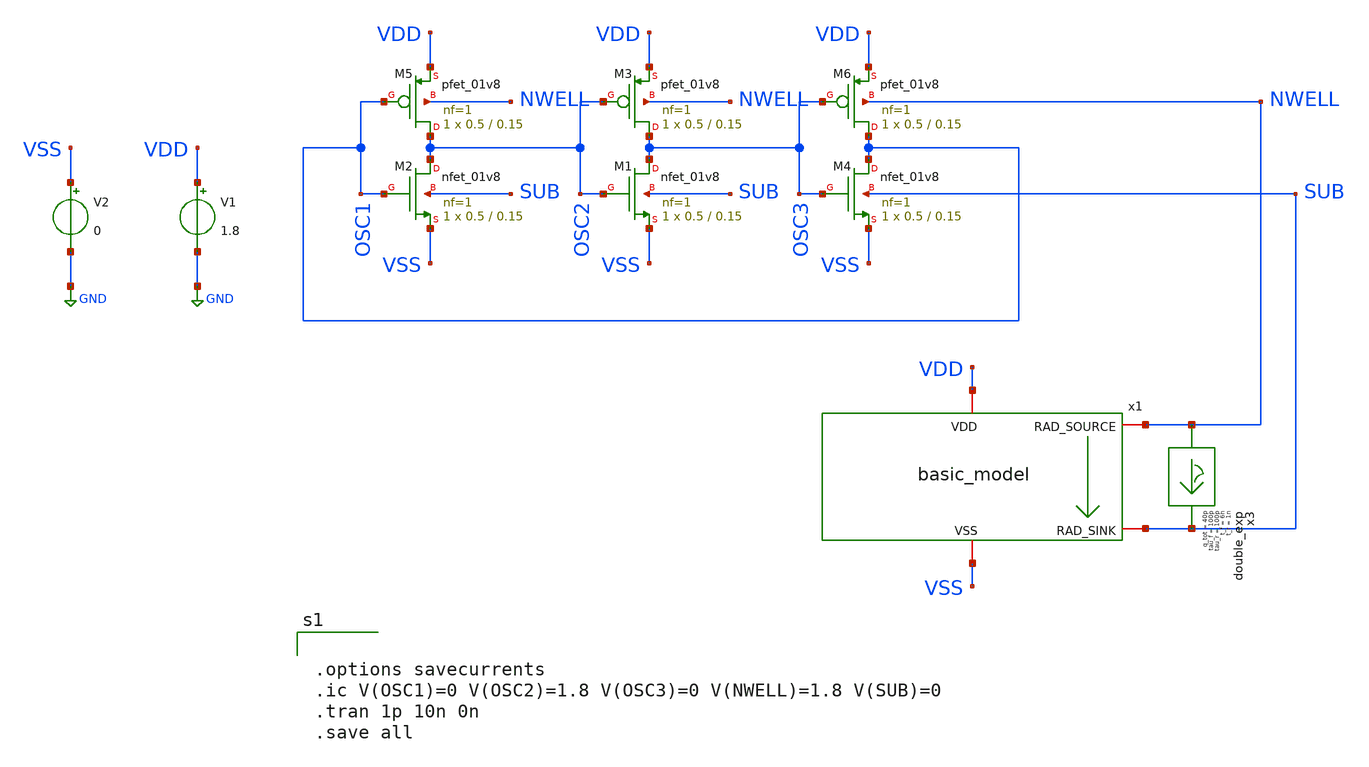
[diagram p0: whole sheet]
** sch_path: untitled-5.sch
**.subckt untitled-5
XM2 OSC2 OSC1 VSS SUB sky130_fd_pr__nfet_01v8 L=0.15 W=0.5 nf=1 ad='int((nf+1)/2) * W/nf * 0.29' as='int((nf+2)/2) * W/nf * 0.29'
+ pd='2*int((nf+1)/2) * (W/nf + 0.29)' ps='2*int((nf+2)/2) * (W/nf + 0.29)' nrd='0.29 / W' nrs='0.29 / W'
+ sa=0 sb=0 sd=0 mult=1 m=1
XM5 OSC2 OSC1 VDD NWELL sky130_fd_pr__pfet_01v8 L=0.15 W=0.5 nf=1 ad='int((nf+1)/2) * W/nf * 0.29' as='int((nf+2)/2) * W/nf * 0.29'
+ pd='2*int((nf+1)/2) * (W/nf + 0.29)' ps='2*int((nf+2)/2) * (W/nf + 0.29)' nrd='0.29 / W' nrs='0.29 / W'
+ sa=0 sb=0 sd=0 mult=1 m=1
XM1 OSC3 OSC2 VSS SUB sky130_fd_pr__nfet_01v8 L=0.15 W=0.5 nf=1 ad='int((nf+1)/2) * W/nf * 0.29' as='int((nf+2)/2) * W/nf * 0.29'
+ pd='2*int((nf+1)/2) * (W/nf + 0.29)' ps='2*int((nf+2)/2) * (W/nf + 0.29)' nrd='0.29 / W' nrs='0.29 / W'
+ sa=0 sb=0 sd=0 mult=1 m=1
XM3 OSC3 OSC2 VDD NWELL sky130_fd_pr__pfet_01v8 L=0.15 W=0.5 nf=1 ad='int((nf+1)/2) * W/nf * 0.29' as='int((nf+2)/2) * W/nf * 0.29'
+ pd='2*int((nf+1)/2) * (W/nf + 0.29)' ps='2*int((nf+2)/2) * (W/nf + 0.29)' nrd='0.29 / W' nrs='0.29 / W'
+ sa=0 sb=0 sd=0 mult=1 m=1
XM4 OSC1 OSC3 VSS SUB sky130_fd_pr__nfet_01v8 L=0.15 W=0.5 nf=1 ad='int((nf+1)/2) * W/nf * 0.29' as='int((nf+2)/2) * W/nf * 0.29'
+ pd='2*int((nf+1)/2) * (W/nf + 0.29)' ps='2*int((nf+2)/2) * (W/nf + 0.29)' nrd='0.29 / W' nrs='0.29 / W'
+ sa=0 sb=0 sd=0 mult=1 m=1
XM6 OSC1 OSC3 VDD NWELL sky130_fd_pr__pfet_01v8 L=0.15 W=0.5 nf=1 ad='int((nf+1)/2) * W/nf * 0.29' as='int((nf+2)/2) * W/nf * 0.29'
+ pd='2*int((nf+1)/2) * (W/nf + 0.29)' ps='2*int((nf+2)/2) * (W/nf + 0.29)' nrd='0.29 / W' nrs='0.29 / W'
+ sa=0 sb=0 sd=0 mult=1 m=1
V1 VDD GND 1.8
V2 VSS GND 0
x3 NWELL SUB double_exp t_r=1n tau_r=100p t_f=6n tau_f=100p q_tot=40p
x1 VDD NWELL SUB VSS basic_model IS_N=1e-18 BF_N=100 VAF_N=50 IKF_N=0.01 CJE_N=0.2p CJC_N=0.1p
+ TF_N=0.2n TR_N=2n IS_P=1e-18 BF_P=100 VAF_P=50 IKF_P=0.01 CJE_P=0.3p CJC_P=0.15p TF_P=0.3n TR_P=3n
**** begin user architecture code


.options savecurrents
.ic V(OSC1)=0 V(OSC2)=1.8 V(OSC3)=0 V(NWELL)=1.8 V(SUB)=0
.tran 1p 10n 0n
.save all



** opencircuitdesign pdks install
.lib $::SKYWATER_MODELS/sky130.lib.spice tt




.include /usr/local/share/rad_modeling_blocks/rad_modeling_blocks.spice


**** end user architecture code
**.ends

* expanding   symbol:  double_exp.sym # of pins=2
** sym_path: xschem_rad_library/double_exp.sym
** sch_path: xschem_rad_library/double_exp.sch
.subckt double_exp in out  t_r=0 t_f=0 tau_r=0 tau_f=0 q_tot=0
*.opin OUT
*.ipin IN
I1 IN OUT EXP(0 {q_tot / (t_f-t_r+tau_f-tau_r)} {t_r} {tau_r} {t_f} {tau_f})
.ends


* expanding   symbol:  OSCRE/latchup/basic_model.sym # of pins=4
** sym_path: latchup/basic_model.sym
** sch_path: latchup/basic_model.sch
.subckt basic_model VDD RAD_SOURCE RAD_SINK VSS   IS_N=1e-16  BF_N=100  VAF_N=100  IKF_N=0.1
+  CJE_N=2p  CJC_N=2p  TF_N=0.1n  TR_N=10n  IS_P=1e-16  BF_P=100  VAF_P=100  IKF_P=0.1  CJE_P=2p  CJC_P=2p
+  TF_P=0.1n  TR_P=10n
*.iopin VDD
*.iopin VSS
*.iopin RAD_SOURCE
*.iopin RAD_SINK
Q1 RAD_SINK RAD_SOURCE VDD pnp_cust area=1 m=1
Q2 RAD_SOURCE RAD_SINK VSS npn_cust area=1 m=1
R3 RAD_SINK VSS 50 m=1
R4 VDD RAD_SOURCE 50 m=1
**** begin user architecture code


.model npn_cust npn (IS={IS_N} BF={BF_N} VAF={VAF_N} IKF={IKF_N} CJE={CJE_N} CJC={CJC_N} TF={TF_N} TR={TR_N})
.model pnp_cust pnp (IS=1e-16 BF=100 VAF=100 IKF=0.1 CJE=2p CJC=2p TF=0.1n TR=10n)


**** end user architecture code
.ends

.GLOBAL GND
.end
